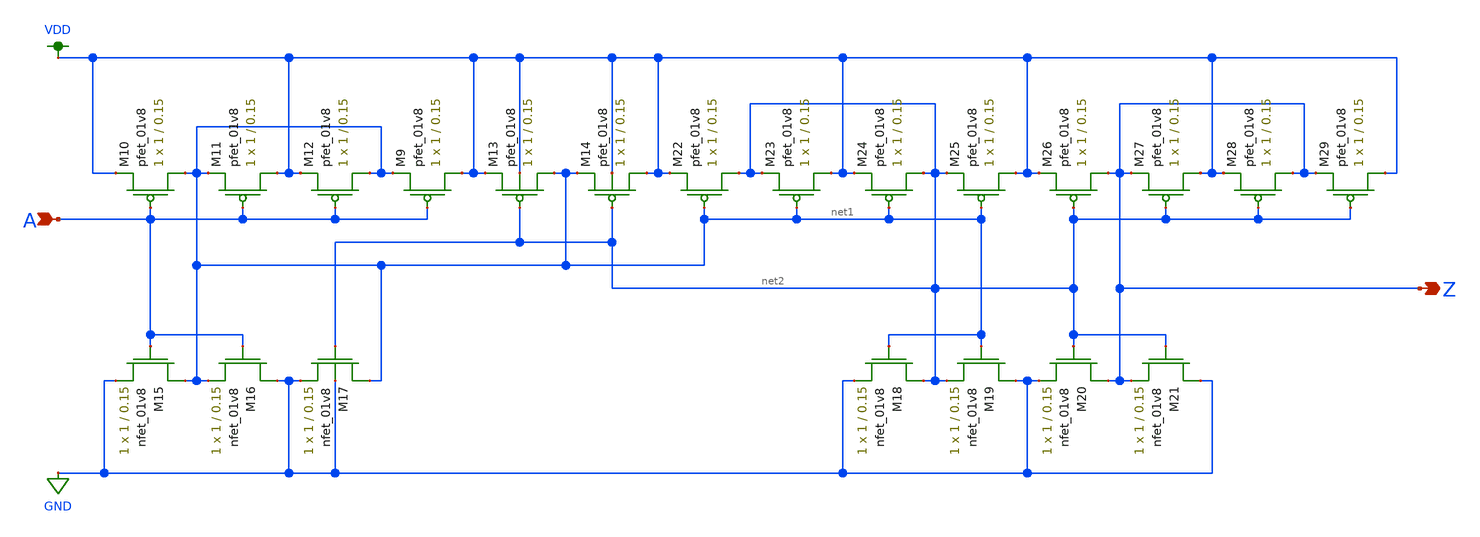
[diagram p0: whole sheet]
** sch_path: schematics/inverter_schmitt_lvs_m.sch
**.subckt inverter_schmitt_lvs_m A Z
*.ipin A
*.opin Z
XM9 VDD A net1 VDD sky130_fd_pr__pfet_01v8 L=0.15 W=1 nf=1 ad='int((nf+1)/2) * W/nf * 0.29' as='int((nf+2)/2) * W/nf * 0.29'
+ pd='2*int((nf+1)/2) * (W/nf + 0.29)' ps='2*int((nf+2)/2) * (W/nf + 0.29)' nrd='0.29 / W' nrs='0.29 / W'
+ sa=0 sb=0 sd=0 mult=1 m=1
XM14 VDD net2 net1 VDD sky130_fd_pr__pfet_01v8 L=0.15 W=1 nf=1 ad='int((nf+1)/2) * W/nf * 0.29' as='int((nf+2)/2) * W/nf * 0.29'
+ pd='2*int((nf+1)/2) * (W/nf + 0.29)' ps='2*int((nf+2)/2) * (W/nf + 0.29)' nrd='0.29 / W' nrs='0.29 / W'
+ sa=0 sb=0 sd=0 mult=1 m=1
XM10 net1 A VDD VDD sky130_fd_pr__pfet_01v8 L=0.15 W=1 nf=1 ad='int((nf+1)/2) * W/nf * 0.29' as='int((nf+2)/2) * W/nf * 0.29'
+ pd='2*int((nf+1)/2) * (W/nf + 0.29)' ps='2*int((nf+2)/2) * (W/nf + 0.29)' nrd='0.29 / W' nrs='0.29 / W'
+ sa=0 sb=0 sd=0 mult=1 m=1
XM11 VDD A net1 VDD sky130_fd_pr__pfet_01v8 L=0.15 W=1 nf=1 ad='int((nf+1)/2) * W/nf * 0.29' as='int((nf+2)/2) * W/nf * 0.29'
+ pd='2*int((nf+1)/2) * (W/nf + 0.29)' ps='2*int((nf+2)/2) * (W/nf + 0.29)' nrd='0.29 / W' nrs='0.29 / W'
+ sa=0 sb=0 sd=0 mult=1 m=1
XM12 net1 A VDD VDD sky130_fd_pr__pfet_01v8 L=0.15 W=1 nf=1 ad='int((nf+1)/2) * W/nf * 0.29' as='int((nf+2)/2) * W/nf * 0.29'
+ pd='2*int((nf+1)/2) * (W/nf + 0.29)' ps='2*int((nf+2)/2) * (W/nf + 0.29)' nrd='0.29 / W' nrs='0.29 / W'
+ sa=0 sb=0 sd=0 mult=1 m=1
XM13 net1 net2 VDD VDD sky130_fd_pr__pfet_01v8 L=0.15 W=1 nf=1 ad='int((nf+1)/2) * W/nf * 0.29' as='int((nf+2)/2) * W/nf * 0.29'
+ pd='2*int((nf+1)/2) * (W/nf + 0.29)' ps='2*int((nf+2)/2) * (W/nf + 0.29)' nrd='0.29 / W' nrs='0.29 / W'
+ sa=0 sb=0 sd=0 mult=1 m=1
XM15 net1 A GND GND sky130_fd_pr__nfet_01v8 L=0.15 W=1 nf=1 ad='int((nf+1)/2) * W/nf * 0.29' as='int((nf+2)/2) * W/nf * 0.29'
+ pd='2*int((nf+1)/2) * (W/nf + 0.29)' ps='2*int((nf+2)/2) * (W/nf + 0.29)' nrd='0.29 / W' nrs='0.29 / W'
+ sa=0 sb=0 sd=0 mult=1 m=1
XM16 GND A net1 GND sky130_fd_pr__nfet_01v8 L=0.15 W=1 nf=1 ad='int((nf+1)/2) * W/nf * 0.29' as='int((nf+2)/2) * W/nf * 0.29'
+ pd='2*int((nf+1)/2) * (W/nf + 0.29)' ps='2*int((nf+2)/2) * (W/nf + 0.29)' nrd='0.29 / W' nrs='0.29 / W'
+ sa=0 sb=0 sd=0 mult=1 m=1
XM17 net1 net2 GND GND sky130_fd_pr__nfet_01v8 L=0.15 W=1 nf=1 ad='int((nf+1)/2) * W/nf * 0.29' as='int((nf+2)/2) * W/nf * 0.29'
+ pd='2*int((nf+1)/2) * (W/nf + 0.29)' ps='2*int((nf+2)/2) * (W/nf + 0.29)' nrd='0.29 / W' nrs='0.29 / W'
+ sa=0 sb=0 sd=0 mult=1 m=1
XM18 net2 net1 GND GND sky130_fd_pr__nfet_01v8 L=0.15 W=1 nf=1 ad='int((nf+1)/2) * W/nf * 0.29' as='int((nf+2)/2) * W/nf * 0.29'
+ pd='2*int((nf+1)/2) * (W/nf + 0.29)' ps='2*int((nf+2)/2) * (W/nf + 0.29)' nrd='0.29 / W' nrs='0.29 / W'
+ sa=0 sb=0 sd=0 mult=1 m=1
XM19 GND net1 net2 GND sky130_fd_pr__nfet_01v8 L=0.15 W=1 nf=1 ad='int((nf+1)/2) * W/nf * 0.29' as='int((nf+2)/2) * W/nf * 0.29'
+ pd='2*int((nf+1)/2) * (W/nf + 0.29)' ps='2*int((nf+2)/2) * (W/nf + 0.29)' nrd='0.29 / W' nrs='0.29 / W'
+ sa=0 sb=0 sd=0 mult=1 m=1
XM20 Z net2 GND GND sky130_fd_pr__nfet_01v8 L=0.15 W=1 nf=1 ad='int((nf+1)/2) * W/nf * 0.29' as='int((nf+2)/2) * W/nf * 0.29'
+ pd='2*int((nf+1)/2) * (W/nf + 0.29)' ps='2*int((nf+2)/2) * (W/nf + 0.29)' nrd='0.29 / W' nrs='0.29 / W'
+ sa=0 sb=0 sd=0 mult=1 m=1
XM21 GND net2 Z GND sky130_fd_pr__nfet_01v8 L=0.15 W=1 nf=1 ad='int((nf+1)/2) * W/nf * 0.29' as='int((nf+2)/2) * W/nf * 0.29'
+ pd='2*int((nf+1)/2) * (W/nf + 0.29)' ps='2*int((nf+2)/2) * (W/nf + 0.29)' nrd='0.29 / W' nrs='0.29 / W'
+ sa=0 sb=0 sd=0 mult=1 m=1
XM22 net2 net1 VDD VDD sky130_fd_pr__pfet_01v8 L=0.15 W=1 nf=1 ad='int((nf+1)/2) * W/nf * 0.29' as='int((nf+2)/2) * W/nf * 0.29'
+ pd='2*int((nf+1)/2) * (W/nf + 0.29)' ps='2*int((nf+2)/2) * (W/nf + 0.29)' nrd='0.29 / W' nrs='0.29 / W'
+ sa=0 sb=0 sd=0 mult=1 m=1
XM23 VDD net1 net2 VDD sky130_fd_pr__pfet_01v8 L=0.15 W=1 nf=1 ad='int((nf+1)/2) * W/nf * 0.29' as='int((nf+2)/2) * W/nf * 0.29'
+ pd='2*int((nf+1)/2) * (W/nf + 0.29)' ps='2*int((nf+2)/2) * (W/nf + 0.29)' nrd='0.29 / W' nrs='0.29 / W'
+ sa=0 sb=0 sd=0 mult=1 m=1
XM24 net2 net1 VDD VDD sky130_fd_pr__pfet_01v8 L=0.15 W=1 nf=1 ad='int((nf+1)/2) * W/nf * 0.29' as='int((nf+2)/2) * W/nf * 0.29'
+ pd='2*int((nf+1)/2) * (W/nf + 0.29)' ps='2*int((nf+2)/2) * (W/nf + 0.29)' nrd='0.29 / W' nrs='0.29 / W'
+ sa=0 sb=0 sd=0 mult=1 m=1
XM25 VDD net1 net2 VDD sky130_fd_pr__pfet_01v8 L=0.15 W=1 nf=1 ad='int((nf+1)/2) * W/nf * 0.29' as='int((nf+2)/2) * W/nf * 0.29'
+ pd='2*int((nf+1)/2) * (W/nf + 0.29)' ps='2*int((nf+2)/2) * (W/nf + 0.29)' nrd='0.29 / W' nrs='0.29 / W'
+ sa=0 sb=0 sd=0 mult=1 m=1
XM26 Z net2 VDD VDD sky130_fd_pr__pfet_01v8 L=0.15 W=1 nf=1 ad='int((nf+1)/2) * W/nf * 0.29' as='int((nf+2)/2) * W/nf * 0.29'
+ pd='2*int((nf+1)/2) * (W/nf + 0.29)' ps='2*int((nf+2)/2) * (W/nf + 0.29)' nrd='0.29 / W' nrs='0.29 / W'
+ sa=0 sb=0 sd=0 mult=1 m=1
XM27 VDD net2 Z VDD sky130_fd_pr__pfet_01v8 L=0.15 W=1 nf=1 ad='int((nf+1)/2) * W/nf * 0.29' as='int((nf+2)/2) * W/nf * 0.29'
+ pd='2*int((nf+1)/2) * (W/nf + 0.29)' ps='2*int((nf+2)/2) * (W/nf + 0.29)' nrd='0.29 / W' nrs='0.29 / W'
+ sa=0 sb=0 sd=0 mult=1 m=1
XM28 Z net2 VDD VDD sky130_fd_pr__pfet_01v8 L=0.15 W=1 nf=1 ad='int((nf+1)/2) * W/nf * 0.29' as='int((nf+2)/2) * W/nf * 0.29'
+ pd='2*int((nf+1)/2) * (W/nf + 0.29)' ps='2*int((nf+2)/2) * (W/nf + 0.29)' nrd='0.29 / W' nrs='0.29 / W'
+ sa=0 sb=0 sd=0 mult=1 m=1
XM29 VDD net2 Z VDD sky130_fd_pr__pfet_01v8 L=0.15 W=1 nf=1 ad='int((nf+1)/2) * W/nf * 0.29' as='int((nf+2)/2) * W/nf * 0.29'
+ pd='2*int((nf+1)/2) * (W/nf + 0.29)' ps='2*int((nf+2)/2) * (W/nf + 0.29)' nrd='0.29 / W' nrs='0.29 / W'
+ sa=0 sb=0 sd=0 mult=1 m=1
**.ends
.GLOBAL VDD
.GLOBAL GND
.end
